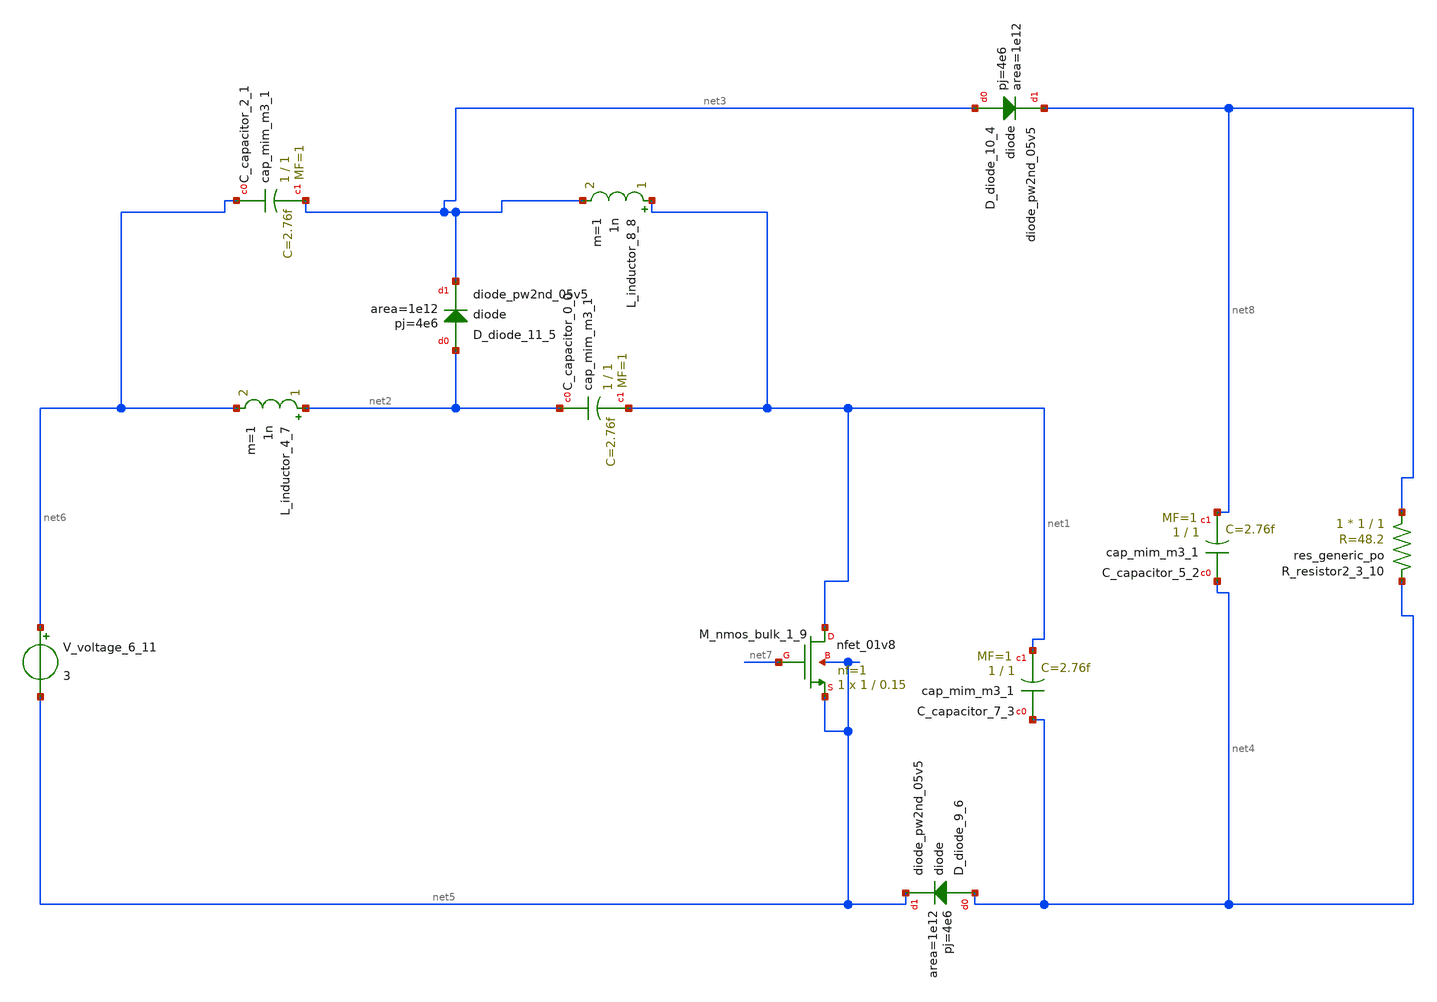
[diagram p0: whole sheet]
** sch_path: schematics/SchemGen/10_1007_s40565-017-0304-1_03_001_crop2.sch
**.subckt 10_1007_s40565-017-0304-1_03_001_crop2
XC_capacitor_0_0 net2 net1 sky130_fd_pr__cap_mim_m3_1 W=1 L=1 MF=1 m=1
XC_capacitor_2_1 net6 net3 sky130_fd_pr__cap_mim_m3_1 W=1 L=1 MF=1 m=1
XC_capacitor_5_2 net4 net8 sky130_fd_pr__cap_mim_m3_1 W=1 L=1 MF=1 m=1
XC_capacitor_7_3 net4 net1 sky130_fd_pr__cap_mim_m3_1 W=1 L=1 MF=1 m=1
XD_diode_10_4 net3 net8 sky130_fd_pr__diode_pw2nd_05v5 area=1e12 pj=4e6
XD_diode_11_5 net2 net3 sky130_fd_pr__diode_pw2nd_05v5 area=1e12 pj=4e6
XD_diode_9_6 net4 net5 sky130_fd_pr__diode_pw2nd_05v5 area=1e12 pj=4e6
L_inductor_4_7 net2 net6 1n m=1
L_inductor_8_8 net1 net3 1n m=1
XM_nmos_bulk_1_9 net1 net7 net5 net5 sky130_fd_pr__nfet_01v8 L=0.15 W=1 nf=1 ad='int((1 + 1)/2) * 1 / 1 * 0.29'
+ as='int((1 + 2)/2) * 1 / 1 * 0.29' pd='2*int((1 + 1)/2) * (1 / 1 + 0.29)' ps='2*int((1 + 2)/2) * (1 / 1 + 0.29)'
+ nrd='0.29 / 1 ' nrs='0.29 / 1 ' sa=0 sb=0 sd=0 mult=1 m=1
XR_resistor2_3_10 net8 net4 sky130_fd_pr__res_generic_po W=1 L=1 m=1
V_voltage_6_11 net6 net5 3
**.ends
.end
